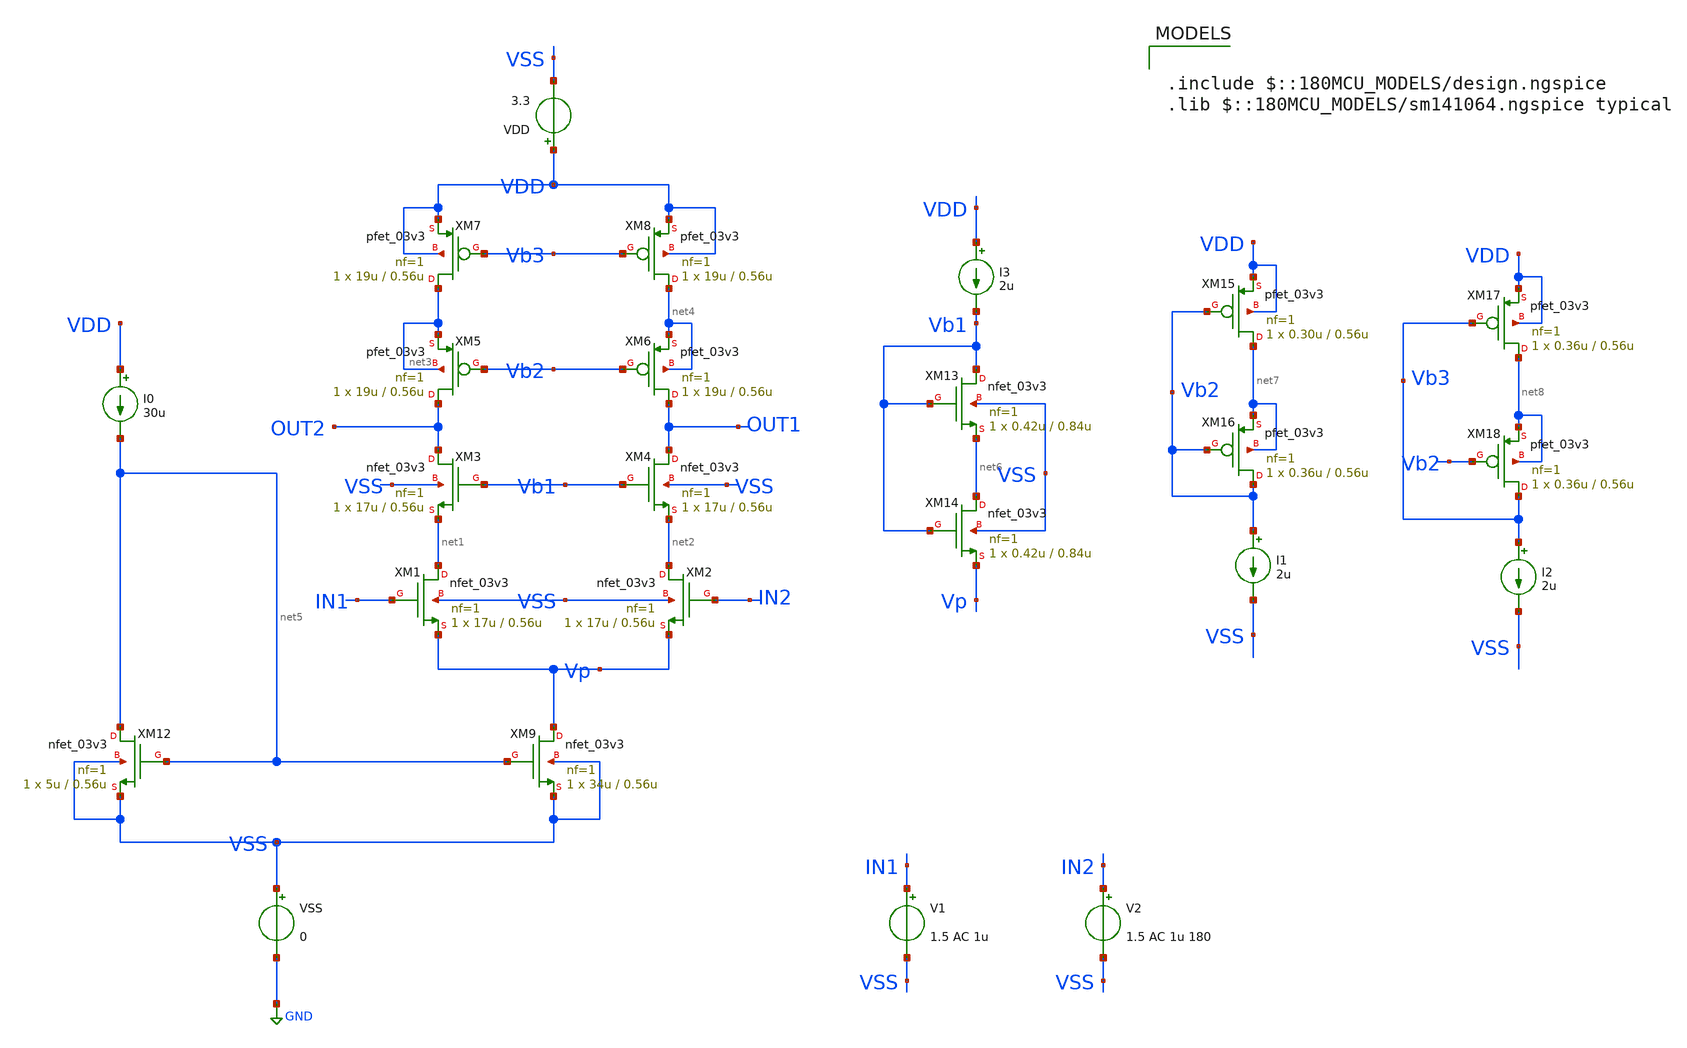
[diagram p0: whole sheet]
** sch_path: SCOP_INPUT_AND_MUX_PAKISTAN_03/Xschem/Others/Diff_Op_Amp.sch
**.subckt Diff_Op_Amp
XM3 OUT2 Vb1 net1 VSS nfet_03v3 L=0.56u W=17u nf=1 ad='int((nf+1)/2) * W/nf * 0.18u' as='int((nf+2)/2) * W/nf * 0.18u'
+ pd='2*int((nf+1)/2) * (W/nf + 0.18u)' ps='2*int((nf+2)/2) * (W/nf + 0.18u)' nrd='0.18u / W' nrs='0.18u / W'
+ sa=0 sb=0 sd=0 m=1
XM4 OUT1 Vb1 net2 VSS nfet_03v3 L=0.56u W=17u nf=1 ad='int((nf+1)/2) * W/nf * 0.18u' as='int((nf+2)/2) * W/nf * 0.18u'
+ pd='2*int((nf+1)/2) * (W/nf + 0.18u)' ps='2*int((nf+2)/2) * (W/nf + 0.18u)' nrd='0.18u / W' nrs='0.18u / W'
+ sa=0 sb=0 sd=0 m=1
XM1 net1 IN1 Vp VSS nfet_03v3 L=0.56u W=17u nf=1 ad='int((nf+1)/2) * W/nf * 0.18u' as='int((nf+2)/2) * W/nf * 0.18u'
+ pd='2*int((nf+1)/2) * (W/nf + 0.18u)' ps='2*int((nf+2)/2) * (W/nf + 0.18u)' nrd='0.18u / W' nrs='0.18u / W'
+ sa=0 sb=0 sd=0 m=1
XM2 net2 IN2 Vp VSS nfet_03v3 L=0.56u W=17u nf=1 ad='int((nf+1)/2) * W/nf * 0.18u' as='int((nf+2)/2) * W/nf * 0.18u'
+ pd='2*int((nf+1)/2) * (W/nf + 0.18u)' ps='2*int((nf+2)/2) * (W/nf + 0.18u)' nrd='0.18u / W' nrs='0.18u / W'
+ sa=0 sb=0 sd=0 m=1
XM5 OUT2 Vb2 net3 net3 pfet_03v3 L=0.56u W=19u nf=1 ad='int((nf+1)/2) * W/nf * 0.18u' as='int((nf+2)/2) * W/nf * 0.18u'
+ pd='2*int((nf+1)/2) * (W/nf + 0.18u)' ps='2*int((nf+2)/2) * (W/nf + 0.18u)' nrd='0.18u / W' nrs='0.18u / W'
+ sa=0 sb=0 sd=0 m=1
XM6 OUT1 Vb2 net4 net4 pfet_03v3 L=0.56u W=19u nf=1 ad='int((nf+1)/2) * W/nf * 0.18u' as='int((nf+2)/2) * W/nf * 0.18u'
+ pd='2*int((nf+1)/2) * (W/nf + 0.18u)' ps='2*int((nf+2)/2) * (W/nf + 0.18u)' nrd='0.18u / W' nrs='0.18u / W'
+ sa=0 sb=0 sd=0 m=1
XM7 net3 Vb3 VDD VDD pfet_03v3 L=0.56u W=19u nf=1 ad='int((nf+1)/2) * W/nf * 0.18u' as='int((nf+2)/2) * W/nf * 0.18u'
+ pd='2*int((nf+1)/2) * (W/nf + 0.18u)' ps='2*int((nf+2)/2) * (W/nf + 0.18u)' nrd='0.18u / W' nrs='0.18u / W'
+ sa=0 sb=0 sd=0 m=1
XM8 net4 Vb3 VDD VDD pfet_03v3 L=0.56u W=19u nf=1 ad='int((nf+1)/2) * W/nf * 0.18u' as='int((nf+2)/2) * W/nf * 0.18u'
+ pd='2*int((nf+1)/2) * (W/nf + 0.18u)' ps='2*int((nf+2)/2) * (W/nf + 0.18u)' nrd='0.18u / W' nrs='0.18u / W'
+ sa=0 sb=0 sd=0 m=1
XM9 Vp net5 VSS VSS nfet_03v3 L=0.56u W=34u nf=1 ad='int((nf+1)/2) * W/nf * 0.18u' as='int((nf+2)/2) * W/nf * 0.18u'
+ pd='2*int((nf+1)/2) * (W/nf + 0.18u)' ps='2*int((nf+2)/2) * (W/nf + 0.18u)' nrd='0.18u / W' nrs='0.18u / W'
+ sa=0 sb=0 sd=0 m=1
XM12 net5 net5 VSS VSS nfet_03v3 L=0.56u W=5u nf=1 ad='int((nf+1)/2) * W/nf * 0.18u' as='int((nf+2)/2) * W/nf * 0.18u'
+ pd='2*int((nf+1)/2) * (W/nf + 0.18u)' ps='2*int((nf+2)/2) * (W/nf + 0.18u)' nrd='0.18u / W' nrs='0.18u / W'
+ sa=0 sb=0 sd=0 m=1
XM13 Vb1 Vb1 net6 VSS nfet_03v3 L=0.84u W=0.42u nf=1 ad='int((nf+1)/2) * W/nf * 0.18u' as='int((nf+2)/2) * W/nf * 0.18u'
+ pd='2*int((nf+1)/2) * (W/nf + 0.18u)' ps='2*int((nf+2)/2) * (W/nf + 0.18u)' nrd='0.18u / W' nrs='0.18u / W'
+ sa=0 sb=0 sd=0 m=1
XM14 net6 Vb1 Vp VSS nfet_03v3 L=0.84u W=0.42u nf=1 ad='int((nf+1)/2) * W/nf * 0.18u' as='int((nf+2)/2) * W/nf * 0.18u'
+ pd='2*int((nf+1)/2) * (W/nf + 0.18u)' ps='2*int((nf+2)/2) * (W/nf + 0.18u)' nrd='0.18u / W' nrs='0.18u / W'
+ sa=0 sb=0 sd=0 m=1
XM15 net7 Vb2 VDD VDD pfet_03v3 L=0.56u W=0.30u nf=1 ad='int((nf+1)/2) * W/nf * 0.18u' as='int((nf+2)/2) * W/nf * 0.18u'
+ pd='2*int((nf+1)/2) * (W/nf + 0.18u)' ps='2*int((nf+2)/2) * (W/nf + 0.18u)' nrd='0.18u / W' nrs='0.18u / W'
+ sa=0 sb=0 sd=0 m=1
XM16 Vb2 Vb2 net7 net7 pfet_03v3 L=0.56u W=0.36u nf=1 ad='int((nf+1)/2) * W/nf * 0.18u' as='int((nf+2)/2) * W/nf * 0.18u'
+ pd='2*int((nf+1)/2) * (W/nf + 0.18u)' ps='2*int((nf+2)/2) * (W/nf + 0.18u)' nrd='0.18u / W' nrs='0.18u / W'
+ sa=0 sb=0 sd=0 m=1
XM17 net8 Vb3 VDD VDD pfet_03v3 L=0.56u W=0.36u nf=1 ad='int((nf+1)/2) * W/nf * 0.18u' as='int((nf+2)/2) * W/nf * 0.18u'
+ pd='2*int((nf+1)/2) * (W/nf + 0.18u)' ps='2*int((nf+2)/2) * (W/nf + 0.18u)' nrd='0.18u / W' nrs='0.18u / W'
+ sa=0 sb=0 sd=0 m=1
XM18 Vb3 Vb2 net8 net8 pfet_03v3 L=0.56u W=0.36u nf=1 ad='int((nf+1)/2) * W/nf * 0.18u' as='int((nf+2)/2) * W/nf * 0.18u'
+ pd='2*int((nf+1)/2) * (W/nf + 0.18u)' ps='2*int((nf+2)/2) * (W/nf + 0.18u)' nrd='0.18u / W' nrs='0.18u / W'
+ sa=0 sb=0 sd=0 m=1
I0 VDD net5 30u
I1 Vb2 VSS 2u
I2 Vb3 VSS 2u
I3 VDD Vb1 2u
VDD VDD VSS 3.3
VSS VSS GND 0
V1 IN1 VSS 1.5 AC 1u
V2 IN2 VSS 1.5 AC 1u 180
**** begin user architecture code

.include $::180MCU_MODELS/design.ngspice
.lib $::180MCU_MODELS/sm141064.ngspice typical




.control
save all @m.xm1.m0[vdsat] @m.xm2.m0[vdsat] @m.xm1.m0[vds] @m.xm2.m0[vds]
save all @m.xm3.m0[vdsat] @m.xm4.m0[vdsat] @m.xm3.m0[vds] @m.xm4.m0[vds]
save all @m.xm5.m0[vdsat] @m.xm6.m0[vdsat] @m.xm5.m0[vds] @m.xm6.m0[vds]
save all @m.xm7.m0[vdsat] @m.xm8.m0[vdsat] @m.xm7.m0[vds] @m.xm8.m0[vds]
save all @m.xm9.m0[vdsat] @m.xm9.m0[vdsat] @m.xm12.m0[vds] @m.xm12.m0[vds]
save all @m.xm1.m0[id] @m.xm2.m0[id] @m.xm3.m0[id] @m.xm4.m0[id]
save all @m.xm9.m0[id] @m.xm10.m0[id] @m.xm11.m0[id] @m.xm12.m0[id]
save all @m.xm10.m0[vdsat] @m.xm11.m0[vdsat] @m.xm10.m0[vds] @m.xm11.m0[vds]
dc V2 1.3 1.7 1m
*ac dec 50 1 100e9
let tf = OUT1/IN1
let gain = db(tf)
let phase = (180/pi)*ph(tf)
*plot gain
*plot phase
let id1 = @m.xm1.m0[id]
let id2 = @m.xm2.m0[id]
let id3 = @m.xm3.m0[id]
let id4 = @m.xm4.m0[id]
*plot id1 id2 id3 id4
let id9 = @m.xm9.m0[id]
let id12 = @m.xm12.m0[id]
*plot id9 id10 id11 id12
let Vov1 = @m.xm1.m0[vdsat]
let Vds1 = @m.xm1.m0[vds]
let Vov2 = @m.xm2.m0[vdsat]
let Vds2 = @m.xm2.m0[vds]
*plot Vov1 Vov2 Vds1 Vds2
let Vov3 = @m.xm3.m0[vdsat]
let Vov4 = @m.xm4.m0[vdsat]
let Vds3 = @m.xm3.m0[vds]
let Vds4 = @m.xm4.m0[vds]
*plot Vov3 Vov4 Vds3 Vds4
let Vov5 = @m.xm5.m0[vdsat]
let Vov6 = @m.xm6.m0[vdsat]
let Vds5 = @m.xm5.m0[vds]
let Vds6 = @m.xm6.m0[vds]
*plot Vov5 Vov6 Vds5 Vds6
let Vov7 = @m.xm7.m0[vdsat]
let Vov8 = @m.xm8.m0[vdsat]
let Vds7 = @m.xm7.m0[vds]
let Vds8 = @m.xm8.m0[vds]
*plot Vov7 Vov8 Vds7 Vds8
let Vov9 = @m.xm9.m0[vdsat]
let Vds9 = @m.xm9.m0[vds]
let Vov12 = @m.xm12.m0[vdsat]
let Vds12 = @m.xm12.m0[vds]
*plot Vov9 Vov12 Vds9 Vds12
let Vov10 = @m.xm10.m0[vdsat]
let Vds10 = @m.xm10.m0[vds]
let Vov11 = @m.xm11.m0[vdsat]
let Vds11 = @m.xm11.m0[vds]
*plot Vov10 Vov11 Vds10 Vds11
*let gds = @m.xm1.m0[gds]
*plot v(Vp) v(Vb1) v(Vb2) v(Vb3)
*plot gds
plot v(OUT1) v(OUT2)
*plot i(VDD)
*write test_nfet_03v3.raw
.endc


**** end user architecture code
**.ends
.GLOBAL GND
.end
